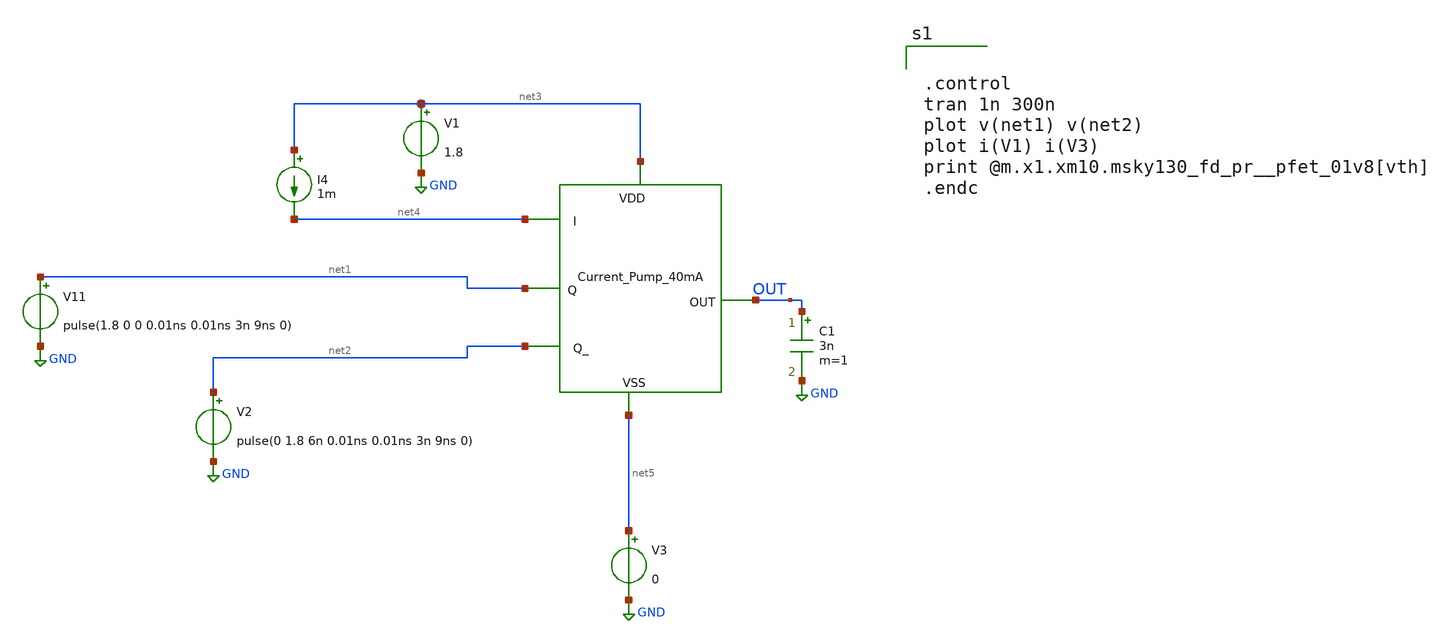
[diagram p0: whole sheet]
** sch_path: xschem/DC_DC_Converter_xschem/DC_DC_Converter/current_pump/current_pump_TB.sch
**.subckt current_pump_TB
V1 net3 GND 1.8
C1 OUT GND 3n m=1
V11 net1 GND pulse(1.8 0 0 0.01ns 0.01ns 3n 9ns 0)
V2 net2 GND pulse(0 1.8 6n 0.01ns 0.01ns 3n 9ns 0)
x1 net4 net3 net5 net1 net2 OUT Current_pump_40mA
I4 net3 net4 1m
V3 net5 GND 0
**** begin user architecture code


.control
tran 1n 300n
plot v(net1) v(net2)
plot i(V1) i(V3)
print @m.x1.xm10.msky130_fd_pr__pfet_01v8[vth]
.endc



** opencircuitdesign pdks install
.lib $::SKYWATER_MODELS/sky130.lib.spice tt


**** end user architecture code
**.ends
.GLOBAL GND
.end
